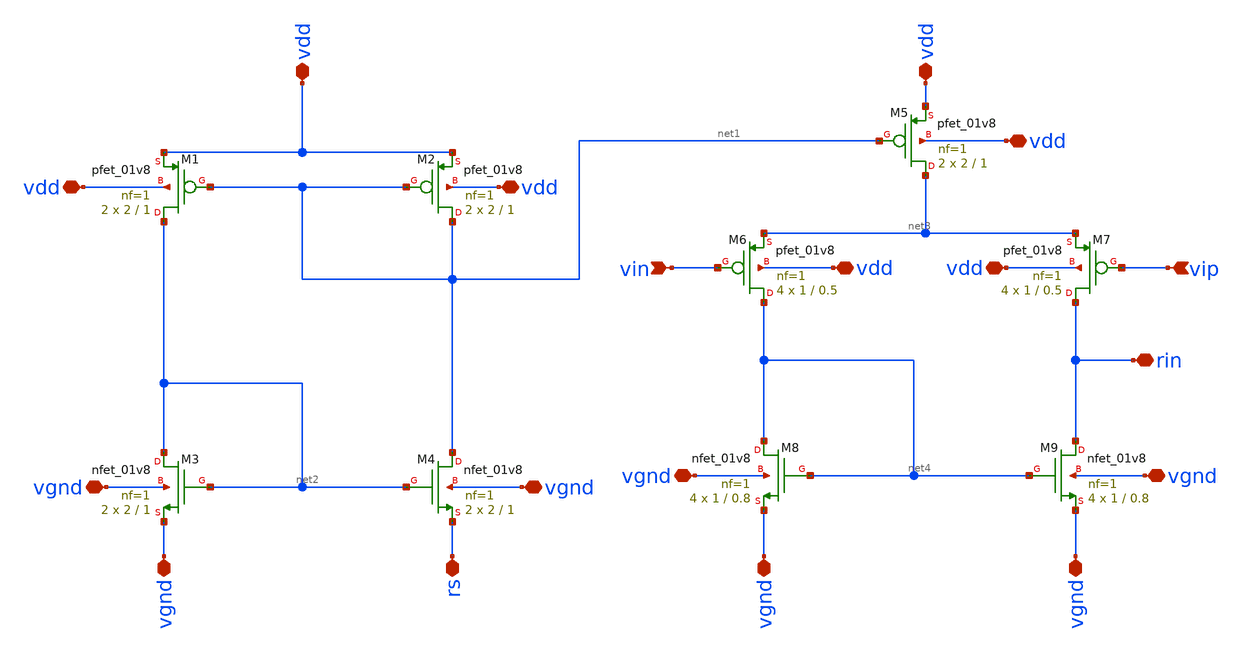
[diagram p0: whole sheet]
** sch_path: xschem/opamp.sch
**.subckt opamp vdd vdd vin vip vgnd vgnd vgnd rs rin vdd vgnd vgnd vgnd vgnd vdd vdd vdd vdd
*.iopin vdd
*.iopin vdd
*.ipin vin
*.ipin vip
*.iopin vgnd
*.iopin vgnd
*.iopin vgnd
*.iopin rs
*.iopin rin
*.iopin vdd
*.iopin vgnd
*.iopin vgnd
*.iopin vgnd
*.iopin vgnd
*.iopin vdd
*.iopin vdd
*.iopin vdd
*.iopin vdd
XM1 net2 net1 vdd vdd sky130_fd_pr__pfet_01v8 L=1 W=2 nf=1 ad='int((nf+1)/2) * W/nf * 0.29' as='int((nf+2)/2) * W/nf * 0.29'
+ pd='2*int((nf+1)/2) * (W/nf + 0.29)' ps='2*int((nf+2)/2) * (W/nf + 0.29)' nrd='0.29 / W' nrs='0.29 / W'
+ sa=0 sb=0 sd=0 mult=2 m=2
XM3 net2 net2 vgnd vgnd sky130_fd_pr__nfet_01v8 L=1 W=2 nf=1 ad='int((nf+1)/2) * W/nf * 0.29' as='int((nf+2)/2) * W/nf * 0.29'
+ pd='2*int((nf+1)/2) * (W/nf + 0.29)' ps='2*int((nf+2)/2) * (W/nf + 0.29)' nrd='0.29 / W' nrs='0.29 / W'
+ sa=0 sb=0 sd=0 mult=2 m=2
XM2 net1 net1 vdd vdd sky130_fd_pr__pfet_01v8 L=1 W=2 nf=1 ad='int((nf+1)/2) * W/nf * 0.29' as='int((nf+2)/2) * W/nf * 0.29'
+ pd='2*int((nf+1)/2) * (W/nf + 0.29)' ps='2*int((nf+2)/2) * (W/nf + 0.29)' nrd='0.29 / W' nrs='0.29 / W'
+ sa=0 sb=0 sd=0 mult=2 m=2
XM4 net1 net2 rs vgnd sky130_fd_pr__nfet_01v8 L=1 W=2 nf=1 ad='int((nf+1)/2) * W/nf * 0.29' as='int((nf+2)/2) * W/nf * 0.29'
+ pd='2*int((nf+1)/2) * (W/nf + 0.29)' ps='2*int((nf+2)/2) * (W/nf + 0.29)' nrd='0.29 / W' nrs='0.29 / W'
+ sa=0 sb=0 sd=0 mult=2 m=2
XM5 net3 net1 vdd vdd sky130_fd_pr__pfet_01v8 L=1 W=2 nf=1 ad='int((nf+1)/2) * W/nf * 0.29' as='int((nf+2)/2) * W/nf * 0.29'
+ pd='2*int((nf+1)/2) * (W/nf + 0.29)' ps='2*int((nf+2)/2) * (W/nf + 0.29)' nrd='0.29 / W' nrs='0.29 / W'
+ sa=0 sb=0 sd=0 mult=2 m=2
XM6 net4 vin net3 vdd sky130_fd_pr__pfet_01v8 L=0.5 W=1 nf=1 ad='int((nf+1)/2) * W/nf * 0.29' as='int((nf+2)/2) * W/nf * 0.29'
+ pd='2*int((nf+1)/2) * (W/nf + 0.29)' ps='2*int((nf+2)/2) * (W/nf + 0.29)' nrd='0.29 / W' nrs='0.29 / W'
+ sa=0 sb=0 sd=0 mult=4 m=4
XM7 rin vip net3 vdd sky130_fd_pr__pfet_01v8 L=0.5 W=1 nf=1 ad='int((nf+1)/2) * W/nf * 0.29' as='int((nf+2)/2) * W/nf * 0.29'
+ pd='2*int((nf+1)/2) * (W/nf + 0.29)' ps='2*int((nf+2)/2) * (W/nf + 0.29)' nrd='0.29 / W' nrs='0.29 / W'
+ sa=0 sb=0 sd=0 mult=4 m=4
XM8 net4 net4 vgnd vgnd sky130_fd_pr__nfet_01v8 L=0.8 W=1 nf=1 ad='int((nf+1)/2) * W/nf * 0.29' as='int((nf+2)/2) * W/nf * 0.29'
+ pd='2*int((nf+1)/2) * (W/nf + 0.29)' ps='2*int((nf+2)/2) * (W/nf + 0.29)' nrd='0.29 / W' nrs='0.29 / W'
+ sa=0 sb=0 sd=0 mult=4 m=4
XM9 rin net4 vgnd vgnd sky130_fd_pr__nfet_01v8 L=0.8 W=1 nf=1 ad='int((nf+1)/2) * W/nf * 0.29' as='int((nf+2)/2) * W/nf * 0.29'
+ pd='2*int((nf+1)/2) * (W/nf + 0.29)' ps='2*int((nf+2)/2) * (W/nf + 0.29)' nrd='0.29 / W' nrs='0.29 / W'
+ sa=0 sb=0 sd=0 mult=4 m=4
**.ends
.end
